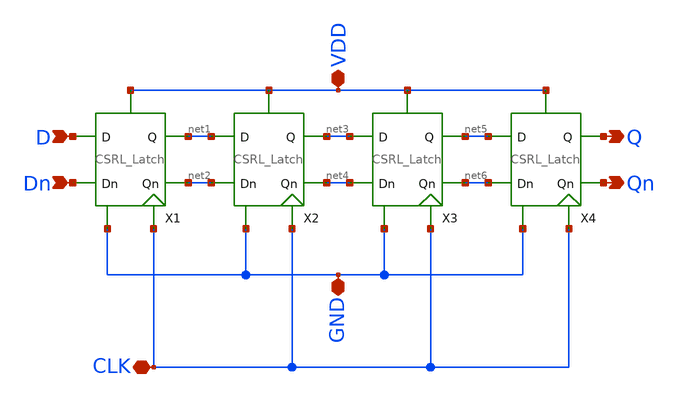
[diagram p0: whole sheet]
** sch_path: shift register/4bit_CSRL.sch
**.subckt 4bit_CSRL Q Qn VDD GND CLK D Dn
*.opin Q
*.opin Qn
*.iopin VDD
*.iopin GND
*.iopin CLK
*.ipin D
*.ipin Dn
X1 D net1 VDD GND CLK Dn net2 CSRL_Latch
X2 net1 net3 VDD GND CLK net2 net4 CSRL_Latch
X3 net3 net5 VDD GND CLK net4 net6 CSRL_Latch
X4 net5 Q VDD GND CLK net6 Qn CSRL_Latch
**.ends
.end
